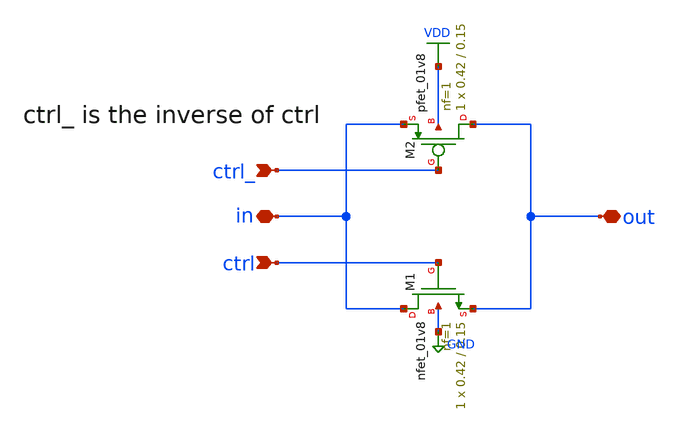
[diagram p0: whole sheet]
** sch_path: xschem/transmission_gate/transmission_gate_set.sch
**.subckt transmission_gate_set in out ctrl_ ctrl
*.iopin in
*.iopin out
*.ipin ctrl_
*.ipin ctrl
XM1 in ctrl out GND sky130_fd_pr__nfet_01v8 L=0.15 W=0.42 nf=1 ad='int((nf+1)/2) * W/nf * 0.29' as='int((nf+2)/2) * W/nf * 0.29'
+ pd='2*int((nf+1)/2) * (W/nf + 0.29)' ps='2*int((nf+2)/2) * (W/nf + 0.29)' nrd='0.29 / W' nrs='0.29 / W'
+ sa=0 sb=0 sd=0 mult=1 m=1
XM2 out ctrl_ in VDD sky130_fd_pr__pfet_01v8 L=0.15 W=0.42 nf=1 ad='int((nf+1)/2) * W/nf * 0.29' as='int((nf+2)/2) * W/nf * 0.29'
+ pd='2*int((nf+1)/2) * (W/nf + 0.29)' ps='2*int((nf+2)/2) * (W/nf + 0.29)' nrd='0.29 / W' nrs='0.29 / W'
+ sa=0 sb=0 sd=0 mult=1 m=1
**.ends
.GLOBAL GND
.GLOBAL VDD
.end
